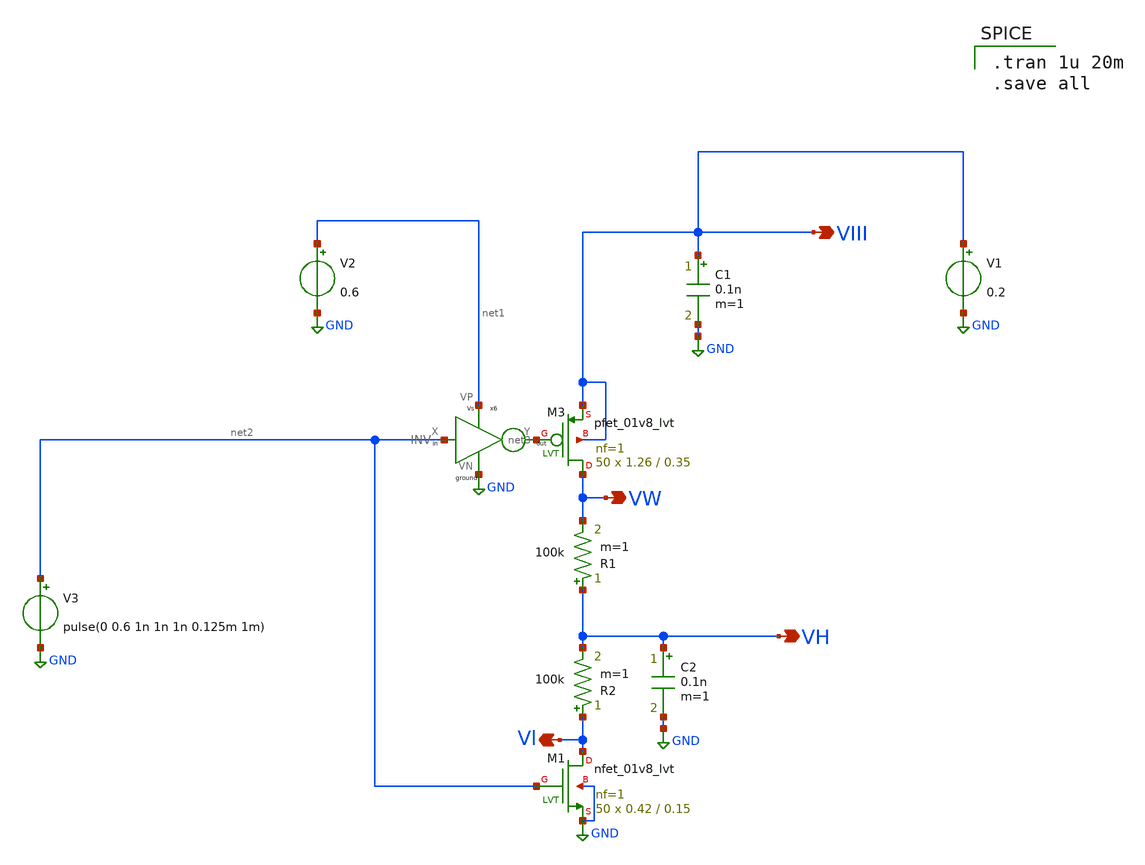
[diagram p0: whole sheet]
** sch_path: untitled-8.sch
**.subckt untitled-8 VIII VH VW Vl
*.opin VIII
*.opin VH
*.opin VW
*.opin Vl
R1 VH VW 100k m=1
R2 Vl VH 100k m=1
XM1 Vl net2 GND GND sky130_fd_pr__nfet_01v8_lvt L=0.15 W=0.42 nf=1 ad='int((nf+1)/2) * W/nf * 0.29' as='int((nf+2)/2) * W/nf * 0.29'
+ pd='2*int((nf+1)/2) * (W/nf + 0.29)' ps='2*int((nf+2)/2) * (W/nf + 0.29)' nrd='0.29 / W' nrs='0.29 / W'
+ sa=0 sb=0 sd=0 mult=50 m=50
x6 net2 net3 net1 GND INV
V2 net1 GND 0.6
V1 VIII GND 0.2
V3 net2 GND pulse(0 0.6 1n 1n 1n 0.125m 1m)
C1 VIII GND 0.1n m=1
C2 VH GND 0.1n m=1
XM3 VW net3 VIII VIII sky130_fd_pr__pfet_01v8_lvt L=0.35 W=1.26 nf=1 ad='int((nf+1)/2) * W/nf * 0.29'
+ as='int((nf+2)/2) * W/nf * 0.29' pd='2*int((nf+1)/2) * (W/nf + 0.29)' ps='2*int((nf+2)/2) * (W/nf + 0.29)'
+ nrd='0.29 / W' nrs='0.29 / W' sa=0 sb=0 sd=0 mult=50 m=50
**** begin user architecture code

** opencircuitdesign pdks install
.lib $::SKYWATER_MODELS/sky130.lib.spice tt



.tran 1u 20m
.save all

**** end user architecture code
**.ends

* expanding   symbol:  pico_chipathon/component/INV/INV.sym # of pins=4
** sym_path: component/INV/INV.sym
** sch_path: component/INV/INV.sch
.subckt INV X Y VP VN
*.ipin X
*.opin Y
*.iopin VN
*.iopin VP
XM1 Y X VN VN sky130_fd_pr__nfet_01v8 L=0.15 W=0.42 nf=1 ad='int((nf+1)/2) * W/nf * 0.29' as='int((nf+2)/2) * W/nf * 0.29'
+ pd='2*int((nf+1)/2) * (W/nf + 0.29)' ps='2*int((nf+2)/2) * (W/nf + 0.29)' nrd='0.29 / W' nrs='0.29 / W'
+ sa=0 sb=0 sd=0 mult=1 m=1
XM2 Y X VP VP sky130_fd_pr__pfet_01v8 L=0.15 W=1.26 nf=1 ad='int((nf+1)/2) * W/nf * 0.29' as='int((nf+2)/2) * W/nf * 0.29'
+ pd='2*int((nf+1)/2) * (W/nf + 0.29)' ps='2*int((nf+2)/2) * (W/nf + 0.29)' nrd='0.29 / W' nrs='0.29 / W'
+ sa=0 sb=0 sd=0 mult=1 m=1
.ends

.GLOBAL GND
.end
